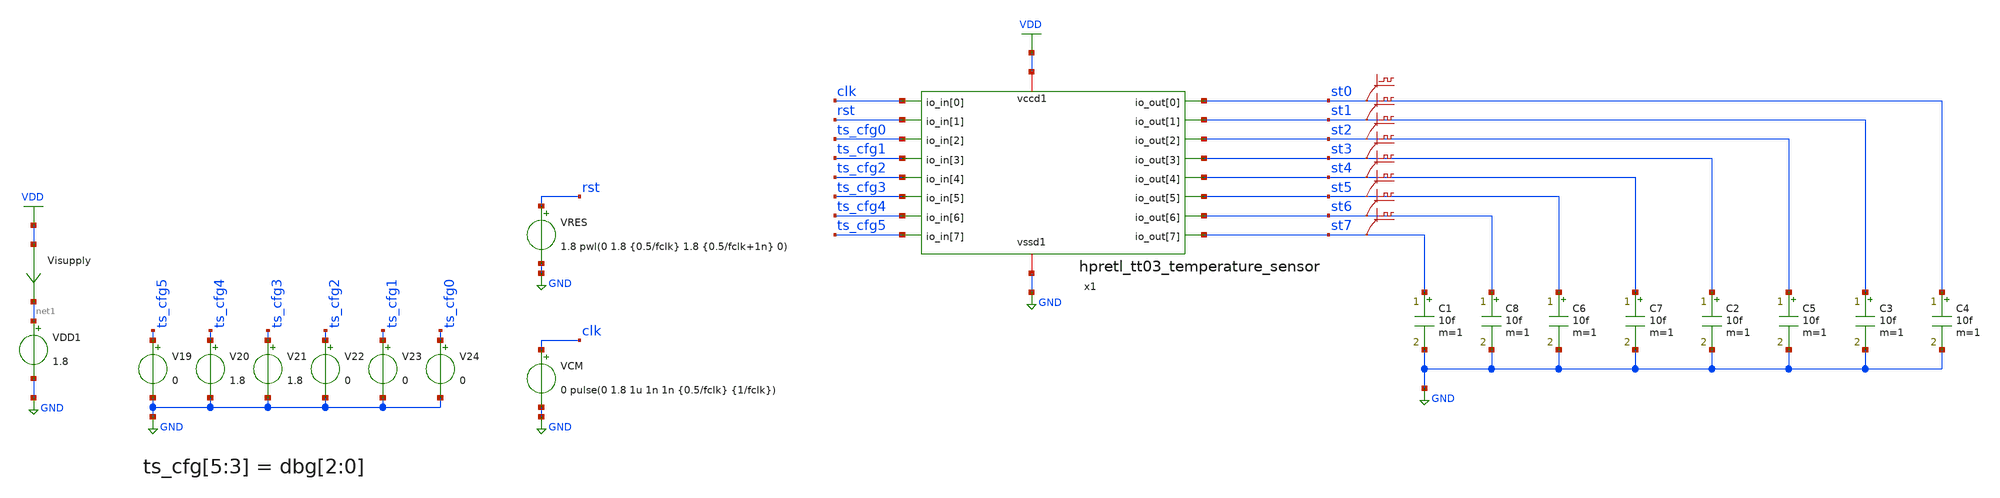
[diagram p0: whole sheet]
** sch_path: sim/tb_tempsens.sch
**.subckt tb_tempsens
VDD1 net1 GND 1.8
V19 ts_cfg5 GND 0
V20 ts_cfg4 GND 1.8
V21 ts_cfg3 GND 1.8
V22 ts_cfg2 GND 0
V23 ts_cfg1 GND 0
V24 ts_cfg0 GND 0
VCM clk GND 0 pulse(0 1.8 1u 1n 1n {0.5/fclk} {1/fclk})
VRES rst GND 1.8 pwl(0 1.8 {0.5/fclk} 1.8 {0.5/fclk+1n} 0)
x1 rst ts_cfg0 ts_cfg1 ts_cfg2 ts_cfg3 ts_cfg4 ts_cfg5 st0 st1 st2 st3 st4 st5 st6 st7 clk VDD GND
+ hpretl_tt03_temperature_sensor
C1 st7 GND 10f m=1
C3 st1 GND 10f m=1
C4 st0 GND 10f m=1
C2 st3 GND 10f m=1
C5 st2 GND 10f m=1
C6 st5 GND 10f m=1
C7 st4 GND 10f m=1
C8 st6 GND 10f m=1
Visupply VDD net1 0
.save i(visupply)
.save v(st0)
.save v(st1)
.save v(st2)
.save v(st3)
.save v(st4)
.save v(st5)
.save v(st6)
.save v(st7)
**** begin user architecture code

** opencircuitdesign pdks install
.lib sky130.lib.spice.tt.red tt





* ngspice commands
****************
.include hpretl_tt03_temperature_sensor_golden.pex.spice

****************
* Misc
****************
.param fclk=10k
.options method=gear maxord=2
.temp 30

.control
tran 10u 30m
*tran 10u 20u

let k=length(time)-1
print st0[k] st1[k] st2[k] st3[k] st4[k] st5[k] st6[k] st7[k] > res.txt

exit
.endc



**** end user architecture code
**.ends
.GLOBAL VDD
.GLOBAL GND
.end
